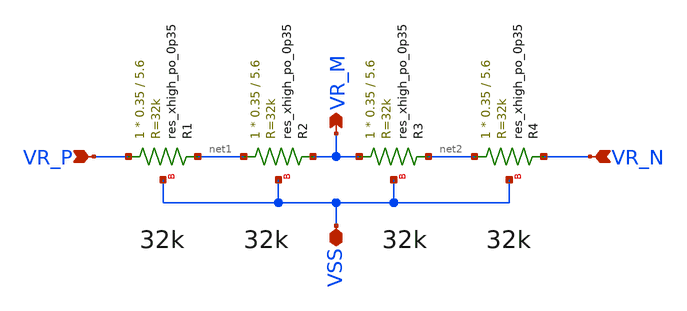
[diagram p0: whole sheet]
** sch_path: xschem/rstring_cm.sch
**.subckt rstring_cm VSS VR_P VR_N VR_M
*.iopin VSS
*.ipin VR_P
*.ipin VR_N
*.opin VR_M
XR1 VR_P net1 VSS sky130_fd_pr__res_xhigh_po_0p35 L=5.6 mult=1 m=1
XR2 net1 VR_M VSS sky130_fd_pr__res_xhigh_po_0p35 L=5.6 mult=1 m=1
XR3 VR_M net2 VSS sky130_fd_pr__res_xhigh_po_0p35 L=5.6 mult=1 m=1
XR4 net2 VR_N VSS sky130_fd_pr__res_xhigh_po_0p35 L=5.6 mult=1 m=1
**.ends
.end
